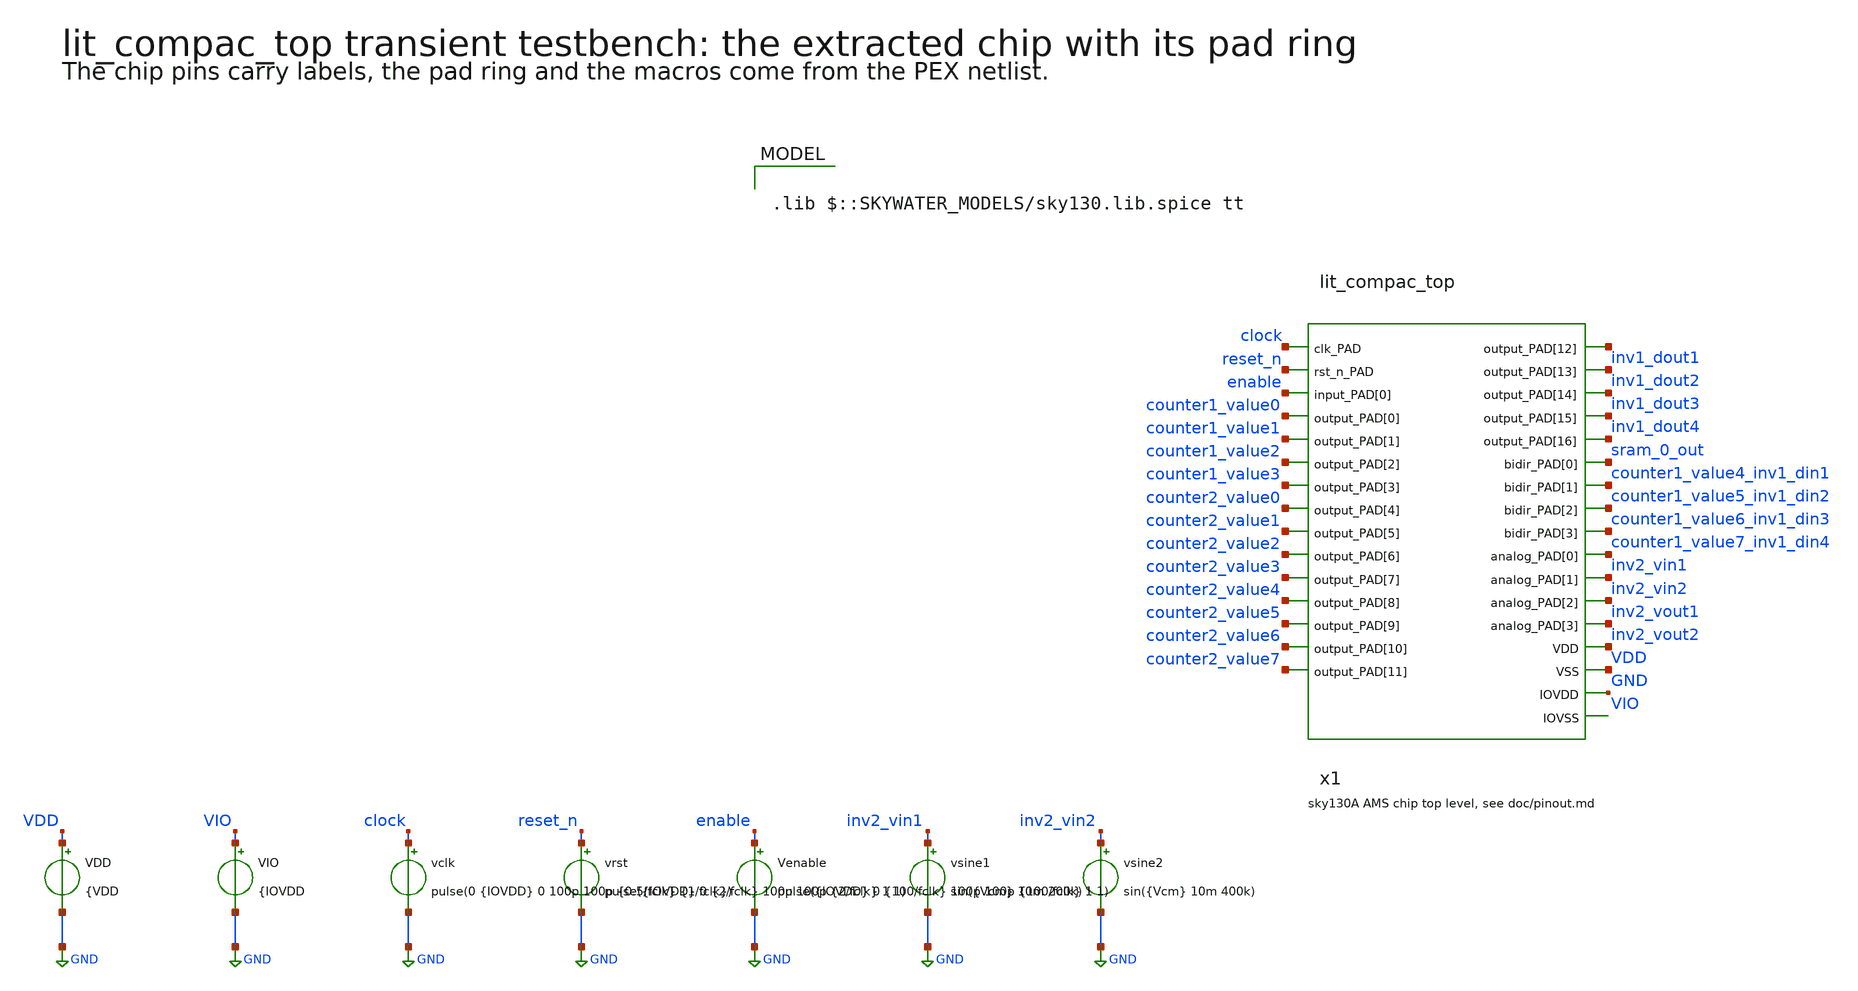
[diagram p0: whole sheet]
** sch_path: testbenches/xschem/lit_compac_top_tb_tran.sch
**.subckt lit_compac_top_tb_tran
x1 clock reset_n enable counter1_value0 counter1_value1 counter1_value2 counter1_value3
+ counter2_value0 counter2_value1 counter2_value2 counter2_value3 counter2_value4 counter2_value5 counter2_value6
+ counter2_value7 inv1_dout1 inv1_dout2 inv1_dout3 inv1_dout4 sram_0_out counter1_value4_inv1_din1
+ counter1_value5_inv1_din2 counter1_value6_inv1_din3 counter1_value7_inv1_din4 inv2_vin1 inv2_vin2 inv2_vout1 inv2_vout2 VDD
+ GND lit_compac_top_pex
VDD VDD GND {VDD
VIO VIO GND {IOVDD
vclk clock GND pulse(0 {IOVDD} 0 100p 100p {0.5/fclk} {1/fclk})
vrst reset_n GND pulse({IOVDD} 0 {2/fclk} 100p 100p {2/fclk} 1 1)
Venable enable GND pulse({IOVDD} 0 {100/fclk} 100p 100p {100/fclk} 1 1)
vsine1 inv2_vin1 GND sin({Vcm} 10m 200k)
vsine2 inv2_vin2 GND sin({Vcm} 10m 400k)
**** begin user architecture code


.include ../../../netlist/pex/lit_compac_top_magic_pex_1.spice
.include ../../../macros/counter/netlist/xspice/counter_top.xspice
.param IOVDD=3.3
.param VDD=1.8
.param Vcm=0.9
.temp 27
.param fclk=40e6
.csparam fclk=fclk
.options klu method=gear reltol=3e-3 vntol=1e-5 abstol=1e-11 chgtol=1e-11 cshunt=100f rshunt=1e15
.control

save all

* User Constants
let tstart = 0
let tstop = 10u
let tstep = 100n

* Transient Operating Point Analysis
op
remzerovec
write @schname.raw
set appendwrite

* Transient Analysis
tran $&tstep $&tstop $&tstart
write @schname.raw

* Plotting
plot clock reset_n enable sram_0_out
plot inv2_vin1 inv2_vout1 inv2_vin2 inv2_vout2
plot inv1_dout1 inv1_dout2 inv1_dout3 inv1_dout4
plot counter2_value0 counter2_value1 counter2_value2 counter2_value3 counter2_value4 counter2_value5
+ counter2_value6 counter2_value7
plot counter1_value4_inv1_din1 counter1_value5_inv1_din2

* Write Data
unset appendwrite
set wr_vecnames
set wr_singlescale
wrdata ../plot_simulations/data/lit_compac_top_tb_tran.txt  v(clock) v(reset_n) v(enable)
+ v(sram_0_out)  v(inv2_vin1) v(inv2_vout1) v(inv2_vin2) v(inv2_vout2)  v(inv1_dout1) v(inv1_dout2) v(inv1_dout3)
+ v(inv1_dout4)  v(counter2_value0) v(counter2_value1) v(counter2_value2) v(counter2_value3)  v(counter2_value4)
+ v(counter2_value5) v(counter2_value6) v(counter2_value7)  v(counter1_value4_inv1_din1) v(counter1_value5_inv1_din2)

*quit
*rusage all
.endc



.lib $::SKYWATER_MODELS/sky130.lib.spice tt

**** end user architecture code
**.ends
.GLOBAL GND
.end
